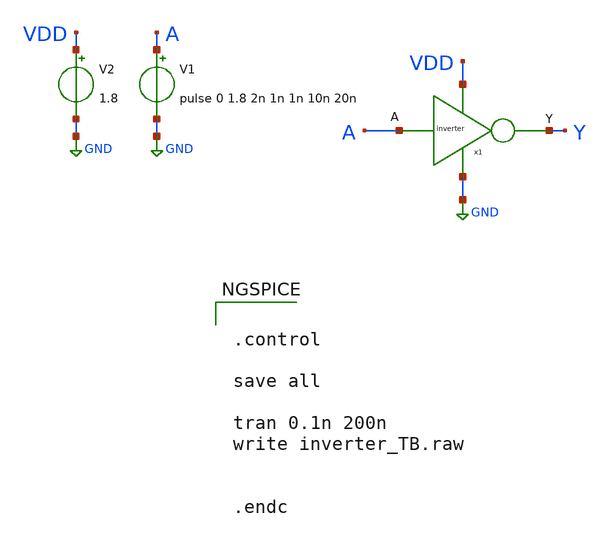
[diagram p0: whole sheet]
** sch_path: inverter/inverter_TB.sch
**.subckt inverter_TB
V1 A GND pulse 0 1.8 2n 1n 1n 10n 20n
V2 VDD GND 1.8
x1 A GND VDD Y inverter
**** begin user architecture code

** opencircuitdesign pdks install
.lib $::SKYWATER_MODELS/sky130.lib.spice tt




.control

save all

tran 0.1n 200n
write inverter_TB.raw


.endc


**** end user architecture code
**.ends

* expanding   symbol:  design/zehra-work/inverter.sym # of pins=4
** sym_path: inverter/inverter.sym
** sch_path: inverter/inverter.sch
.subckt inverter A VSS VDD Y
*.iopin VDD
*.iopin VSS
*.iopin A
*.iopin Y
XM3 Y A VSS VSS sky130_fd_pr__nfet_01v8_lvt L=0.15 W=1 nf=1 ad='int((nf+1)/2) * W/nf * 0.29' as='int((nf+2)/2) * W/nf * 0.29'
+ pd='2*int((nf+1)/2) * (W/nf + 0.29)' ps='2*int((nf+2)/2) * (W/nf + 0.29)' nrd='0.29 / W' nrs='0.29 / W'
+ sa=0 sb=0 sd=0 mult=1 m=1
XM1 Y A VDD VDD sky130_fd_pr__pfet_01v8_lvt L=0.35 W=1 nf=1 ad='int((nf+1)/2) * W/nf * 0.29' as='int((nf+2)/2) * W/nf * 0.29'
+ pd='2*int((nf+1)/2) * (W/nf + 0.29)' ps='2*int((nf+2)/2) * (W/nf + 0.29)' nrd='0.29 / W' nrs='0.29 / W'
+ sa=0 sb=0 sd=0 mult=1 m=1
.ends

.GLOBAL GND
.end
